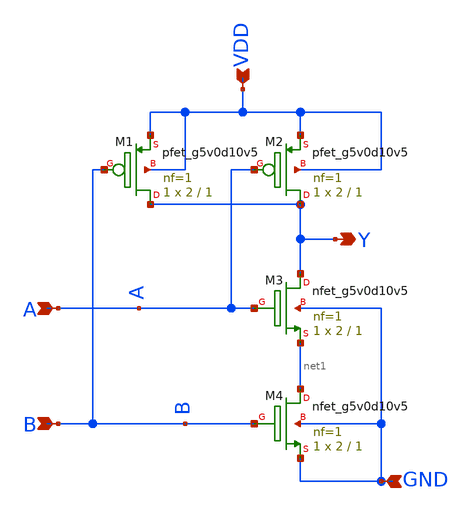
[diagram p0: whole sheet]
** sch_path: ADC/16bit_C2C/MagicAndSpice/EE431_FinalProj/NAND2_5V.sch
**.subckt NAND2_5V A B VDD GND Y
*.ipin A
*.ipin B
*.ipin VDD
*.ipin GND
*.opin Y
XM1 Y B VDD VDD sky130_fd_pr__pfet_g5v0d10v5 L=1 W=2 nf=1 ad='int((nf+1)/2) * W/nf * 0.29' as='int((nf+2)/2) * W/nf * 0.29'
+ pd='2*int((nf+1)/2) * (W/nf + 0.29)' ps='2*int((nf+2)/2) * (W/nf + 0.29)' nrd='0.29 / W' nrs='0.29 / W'
+ sa=0 sb=0 sd=0 mult=1 m=1
XM2 Y A VDD VDD sky130_fd_pr__pfet_g5v0d10v5 L=1 W=2 nf=1 ad='int((nf+1)/2) * W/nf * 0.29' as='int((nf+2)/2) * W/nf * 0.29'
+ pd='2*int((nf+1)/2) * (W/nf + 0.29)' ps='2*int((nf+2)/2) * (W/nf + 0.29)' nrd='0.29 / W' nrs='0.29 / W'
+ sa=0 sb=0 sd=0 mult=1 m=1
XM3 Y A net1 GND sky130_fd_pr__nfet_g5v0d10v5 L=1 W=2 nf=1 ad='int((nf+1)/2) * W/nf * 0.29' as='int((nf+2)/2) * W/nf * 0.29'
+ pd='2*int((nf+1)/2) * (W/nf + 0.29)' ps='2*int((nf+2)/2) * (W/nf + 0.29)' nrd='0.29 / W' nrs='0.29 / W'
+ sa=0 sb=0 sd=0 mult=1 m=1
XM4 net1 B GND GND sky130_fd_pr__nfet_g5v0d10v5 L=1 W=2 nf=1 ad='int((nf+1)/2) * W/nf * 0.29' as='int((nf+2)/2) * W/nf * 0.29'
+ pd='2*int((nf+1)/2) * (W/nf + 0.29)' ps='2*int((nf+2)/2) * (W/nf + 0.29)' nrd='0.29 / W' nrs='0.29 / W'
+ sa=0 sb=0 sd=0 mult=1 m=1
**.ends
.end
